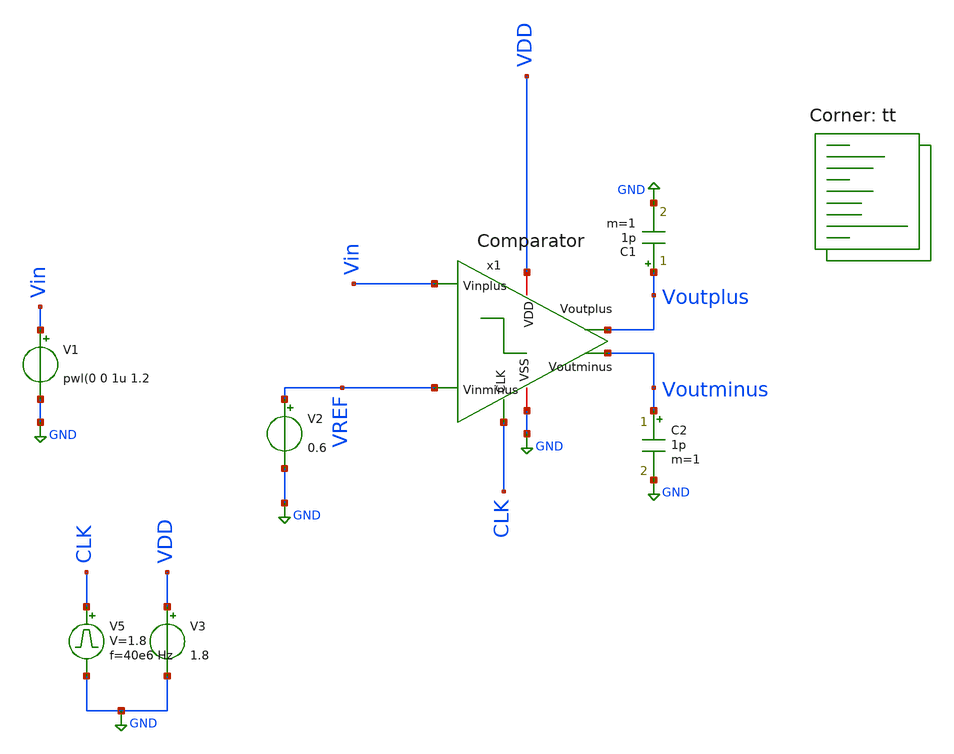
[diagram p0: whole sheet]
** sch_path: ComparatorTB.sch
**.subckt ComparatorTB
V2 VREF GND 0.6
V3 VDD GND 1.8
.save i(v3)
V1 Vin GND pwl(0 0 1u 1.2
C1 Voutplus GND 1p m=1
C2 Voutminus GND 1p m=1
V5 CLK GND pulse 0 1.8 '0.495/ 40e6 ' '0.01/40e6 ' '0.01/40e6 ' '0.49/40e6 ' '1/40e6 '
x1 VDD Voutminus Voutplus CLK Vin VREF GND Comparator
**** begin user architecture code


.savecurrents
.control
 save all
 op
 print x1.Viominus x1.Vioplus
 print @m.x1.xm11.msky130_fd_pr__pfet_01v8_lvt[id]
 print @m.x1.xm11.msky130_fd_pr__pfet_01v8_lvt[vds] - @m.x1.xm11.msky130_fd_pr__pfet_01v8_lvt[vth]
 print @m.x1.xm11.msky130_fd_pr__pfet_01v8_lvt[gm]
 tran 1e-9 1u

 plot Voutplus Voutminus
 plot x1.VoutplusB x1.VoutminusB
 plot Vin CLK
 plot Vin


 let Vdif = Vin - Vref
 let Voutdiff= Voutplus-Voutminus
 *plot Vdif Voutdiff
 plot i(V3)
 plot x1.Viominus x1.Vioplus

 write ComparatorTB.raw
.endc


.lib $::SKYWATER_MODELS/sky130.lib.spice tt
Cgg = 1.021899e-14
**** end user architecture code
**.ends
.GLOBAL GND
.end
